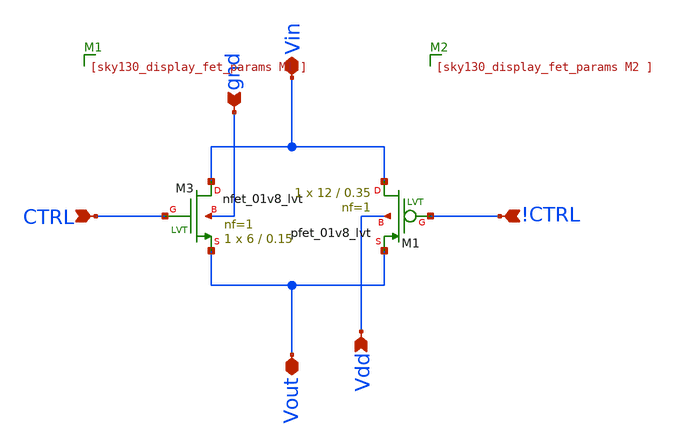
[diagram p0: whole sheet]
** sch_path: 05_mixed_signal/soluzioni/lab03/xschem/passgate.sch
**.subckt passgate CTRL !CTRL Vin Vout Vdd gnd
*.ipin CTRL
*.ipin !CTRL
*.iopin Vin
*.iopin Vout
*.ipin Vdd
*.ipin gnd
XM3 Vin CTRL Vout gnd sky130_fd_pr__nfet_01v8_lvt L=0.15 W=6 nf=1 ad='int((1 + 1)/2) * 6 / 1 * 0.29'
+ as='int((1 + 2)/2) * 6 / 1 * 0.29' pd='2*int((1 + 1)/2) * (6 / 1 + 0.29)' ps='2*int((1 + 2)/2) * (6 / 1 + 0.29)'
+ nrd='0.29 / 6 ' nrs='0.29 / 6 ' sa=0 sb=0 sd=0 mult=1 m=1
XM1 Vin !CTRL Vout Vdd sky130_fd_pr__pfet_01v8_lvt L=0.35 W=12 nf=1 ad='int((1 + 1)/2) * 12 / 1 * 0.29'
+ as='int((1 + 2)/2) * 12 / 1 * 0.29' pd='2*int((1 + 1)/2) * (12 / 1 + 0.29)' ps='2*int((1 + 2)/2) * (12 / 1 + 0.29)'
+ nrd='0.29 / 12 ' nrs='0.29 / 12 ' sa=0 sb=0 sd=0 mult=1 m=1
**.ends
.end
